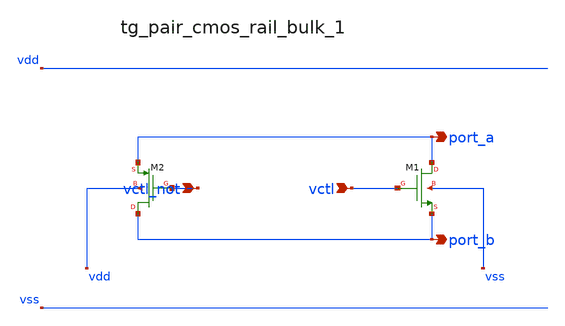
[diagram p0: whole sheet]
** sch_path: analog-db/raw/sw_001_transmission_gate_pair/hier/blocks/tg_pair_cmos_rail_bulk_1.sch
**.subckt tg_pair_cmos_rail_bulk_1 vctl_not vctl port_a port_b
*.ipin vctl_not
*.ipin vctl
*.opin port_a
*.opin port_b
XM1 port_a vctl port_b vss sg13_lv_nmos w=x_dut_xm1_w l=x_dut_xm1_l ng=1 m=x_dut_xm1_m
XM2 port_b vctl_not port_a vdd sg13_lv_pmos w=x_dut_xm2_w l=x_dut_xm2_l ng=1 m=x_dut_xm2_m
**.ends
.end
